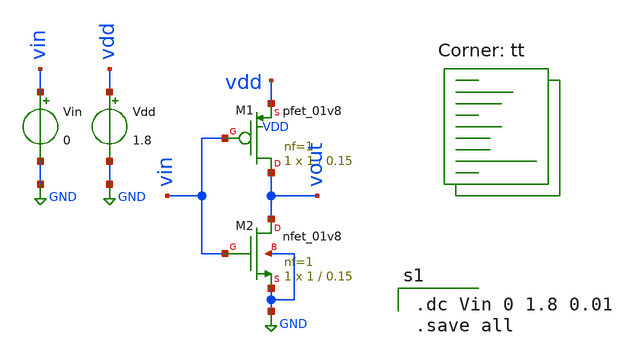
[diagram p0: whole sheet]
** sch_path: xschem/inverter.sch
**.subckt inverter
XM1 vout vin vdd VDD sky130_fd_pr__pfet_01v8 L=0.15 W=1 nf=1 ad='int((1 + 1)/2) * 1 / 1 * 0.29' as='int((1 + 2)/2) * 1 / 1 * 0.29'
+ pd='2*int((1 + 1)/2) * (1 / 1 + 0.29)' ps='2*int((1 + 2)/2) * (1 / 1 + 0.29)' nrd='0.29 / 1 ' nrs='0.29 / 1 '
+ sa=0 sb=0 sd=0 mult=1 m=1
XM2 vout vin GND GND sky130_fd_pr__nfet_01v8 L=0.15 W=1 nf=1 ad='int((1 + 1)/2) * 1 / 1 * 0.29' as='int((1 + 2)/2) * 1 / 1 * 0.29'
+ pd='2*int((1 + 1)/2) * (1 / 1 + 0.29)' ps='2*int((1 + 2)/2) * (1 / 1 + 0.29)' nrd='0.29 / 1 ' nrs='0.29 / 1 '
+ sa=0 sb=0 sd=0 mult=1 m=1
Vdd vdd GND 1.8
Vin vin GND 0
**** begin user architecture code

.dc Vin 0 1.8 0.01
.save all

.lib $::SKYWATER_MODELS/sky130.lib.spice tt
**** end user architecture code
**.ends
.GLOBAL GND
.end
